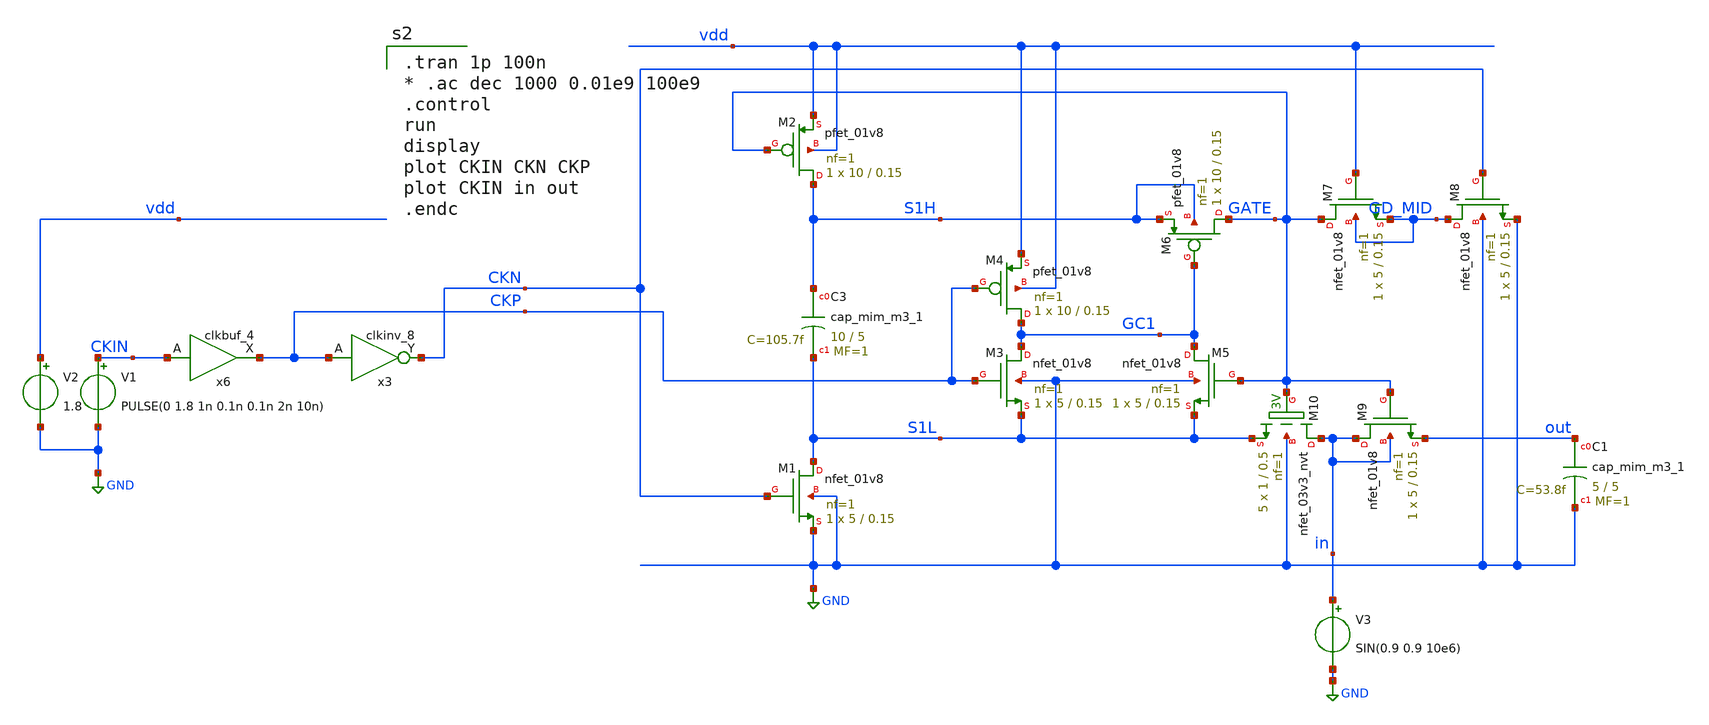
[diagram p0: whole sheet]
** sch_path: xschem/snh_complete1.sch
**.subckt snh_complete1
V1 CKIN GND PULSE(0 1.8 1n 0.1n 0.1n 2n 10n)
V2 vdd GND 1.8
XC3 S1H S1L sky130_fd_pr__cap_mim_m3_1 W=10 L=5 MF=1 m=1
XM1 S1L CKN GND GND sky130_fd_pr__nfet_01v8 L=0.15 W=5 nf=1 ad='int((nf+1)/2) * W/nf * 0.29' as='int((nf+2)/2) * W/nf * 0.29'
+ pd='2*int((nf+1)/2) * (W/nf + 0.29)' ps='2*int((nf+2)/2) * (W/nf + 0.29)' nrd='0.29 / W' nrs='0.29 / W'
+ sa=0 sb=0 sd=0 mult=1 m=1
XM3 GC1 CKP S1L GND sky130_fd_pr__nfet_01v8 L=0.15 W=5 nf=1 ad='int((nf+1)/2) * W/nf * 0.29' as='int((nf+2)/2) * W/nf * 0.29'
+ pd='2*int((nf+1)/2) * (W/nf + 0.29)' ps='2*int((nf+2)/2) * (W/nf + 0.29)' nrd='0.29 / W' nrs='0.29 / W'
+ sa=0 sb=0 sd=0 mult=1 m=1
XM4 GC1 CKP vdd vdd sky130_fd_pr__pfet_01v8 L=0.15 W=10 nf=1 ad='int((nf+1)/2) * W/nf * 0.29' as='int((nf+2)/2) * W/nf * 0.29'
+ pd='2*int((nf+1)/2) * (W/nf + 0.29)' ps='2*int((nf+2)/2) * (W/nf + 0.29)' nrd='0.29 / W' nrs='0.29 / W'
+ sa=0 sb=0 sd=0 mult=1 m=1
XM5 GC1 GATE S1L GND sky130_fd_pr__nfet_01v8 L=0.15 W=5 nf=1 ad='int((nf+1)/2) * W/nf * 0.29' as='int((nf+2)/2) * W/nf * 0.29'
+ pd='2*int((nf+1)/2) * (W/nf + 0.29)' ps='2*int((nf+2)/2) * (W/nf + 0.29)' nrd='0.29 / W' nrs='0.29 / W'
+ sa=0 sb=0 sd=0 mult=1 m=1
XM6 GATE GC1 S1H S1H sky130_fd_pr__pfet_01v8 L=0.15 W=10 nf=1 ad='int((nf+1)/2) * W/nf * 0.29' as='int((nf+2)/2) * W/nf * 0.29'
+ pd='2*int((nf+1)/2) * (W/nf + 0.29)' ps='2*int((nf+2)/2) * (W/nf + 0.29)' nrd='0.29 / W' nrs='0.29 / W'
+ sa=0 sb=0 sd=0 mult=1 m=1
XM7 GATE vdd GD_MID GD_MID sky130_fd_pr__nfet_01v8 L=0.15 W=5 nf=1 ad='int((nf+1)/2) * W/nf * 0.29' as='int((nf+2)/2) * W/nf * 0.29'
+ pd='2*int((nf+1)/2) * (W/nf + 0.29)' ps='2*int((nf+2)/2) * (W/nf + 0.29)' nrd='0.29 / W' nrs='0.29 / W'
+ sa=0 sb=0 sd=0 mult=1 m=1
XM8 GD_MID CKN GND GND sky130_fd_pr__nfet_01v8 L=0.15 W=5 nf=1 ad='int((nf+1)/2) * W/nf * 0.29' as='int((nf+2)/2) * W/nf * 0.29'
+ pd='2*int((nf+1)/2) * (W/nf + 0.29)' ps='2*int((nf+2)/2) * (W/nf + 0.29)' nrd='0.29 / W' nrs='0.29 / W'
+ sa=0 sb=0 sd=0 mult=1 m=1
V3 in GND SIN(0.9 0.9 10e6)
x3 CKP gnd gnd vdd vdd CKN sky130_fd_sc_hd__clkinv_8
x6 CKIN gnd gnd vdd vdd CKP sky130_fd_sc_hd__clkbuf_4
XM2 S1H GATE vdd vdd sky130_fd_pr__pfet_01v8 L=0.15 W=10 nf=1 ad='int((nf+1)/2) * W/nf * 0.29' as='int((nf+2)/2) * W/nf * 0.29'
+ pd='2*int((nf+1)/2) * (W/nf + 0.29)' ps='2*int((nf+2)/2) * (W/nf + 0.29)' nrd='0.29 / W' nrs='0.29 / W'
+ sa=0 sb=0 sd=0 mult=1 m=1
XC1 out GND sky130_fd_pr__cap_mim_m3_1 W=5 L=5 MF=1 m=1
XM10 in GATE S1L GND sky130_fd_pr__nfet_03v3_nvt L=0.5 W=1 nf=1 ad='int((nf+1)/2) * W/nf * 0.29' as='int((nf+2)/2) * W/nf * 0.29'
+ pd='2*int((nf+1)/2) * (W/nf + 0.29)' ps='2*int((nf+2)/2) * (W/nf + 0.29)' nrd='0.29 / W' nrs='0.29 / W'
+ sa=0 sb=0 sd=0 mult=5 m=5
XM9 in GATE out in sky130_fd_pr__nfet_01v8 L=0.15 W=5 nf=1 ad='int((nf+1)/2) * W/nf * 0.29' as='int((nf+2)/2) * W/nf * 0.29'
+ pd='2*int((nf+1)/2) * (W/nf + 0.29)' ps='2*int((nf+2)/2) * (W/nf + 0.29)' nrd='0.29 / W' nrs='0.29 / W'
+ sa=0 sb=0 sd=0 mult=1 m=1
**** begin user architecture code
.lib $::SKYWATER_MODELS/sky130.lib.spice tt
.include /home/al/openmpw/pdk_1/sky130B/libs.ref/sky130_fd_sc_hd/spice/sky130_fd_sc_hd.spice


.tran 1p 100n
* .ac dec 1000 0.01e9 100e9
.control
run
display
plot CKIN CKN CKP
plot CKIN in out
.endc


**** end user architecture code
**.ends
.GLOBAL GND
.end
